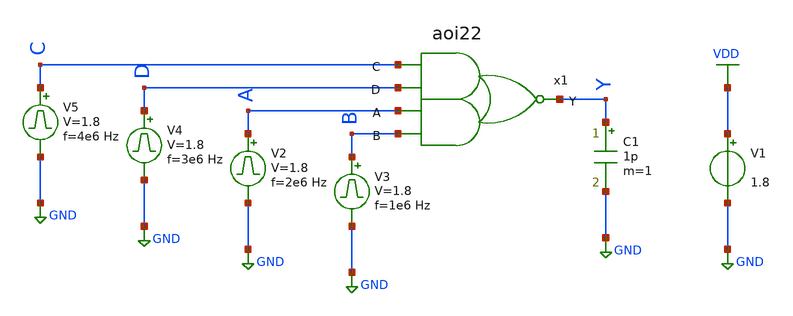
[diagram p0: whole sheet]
** sch_path: library/xschem/aoi22_tb.sch
**.subckt aoi22_tb
V1 VDD GND 1.8
V2 A GND pulse 0 1.8 '0.495/ 2e6 ' '0.01/2e6 ' '0.01/2e6 ' '0.49/2e6 ' '1/2e6 '
C1 Y GND 1p m=1
V3 B GND pulse 0 1.8 '0.495/ 1e6 ' '0.01/1e6 ' '0.01/1e6 ' '0.49/1e6 ' '1/1e6 '
V4 D GND pulse 0 1.8 '0.495/ 3e6 ' '0.01/3e6 ' '0.01/3e6 ' '0.49/3e6 ' '1/3e6 '
V5 C GND pulse 0 1.8 '0.495/ 4e6 ' '0.01/4e6 ' '0.01/4e6 ' '0.49/4e6 ' '1/4e6 '
x1 C D A Y B aoi22
**** begin user architecture code


.control
save all
tran 1n 2u
plot V(A) V(B)+2 V(C)+4 V(D)+6 V(Y)+8
.endc


** opencircuitdesign pdks install
.lib $::SKYWATER_MODELS/sky130.lib.spice tt


**** end user architecture code
**.ends

* expanding   symbol:  aoi22.sym # of pins=5
** sym_path: library/xschem/aoi22.sym
** sch_path: library/xschem/aoi22.sch
.subckt aoi22 C D A Y B
*.opin Y
*.ipin C
*.ipin D
*.ipin A
*.ipin B
XM1 Y A net2 GND sky130_fd_pr__nfet_01v8 L=0.15 W=1 nf=1 ad='int((nf+1)/2) * W/nf * 0.29' as='int((nf+2)/2) * W/nf * 0.29'
+ pd='2*int((nf+1)/2) * (W/nf + 0.29)' ps='2*int((nf+2)/2) * (W/nf + 0.29)' nrd='0.29 / W' nrs='0.29 / W'
+ sa=0 sb=0 sd=0 mult=1 m=1
XM2 net1 A VDD VDD sky130_fd_pr__pfet_01v8 L=0.15 W=1 nf=1 ad='int((nf+1)/2) * W/nf * 0.29' as='int((nf+2)/2) * W/nf * 0.29'
+ pd='2*int((nf+1)/2) * (W/nf + 0.29)' ps='2*int((nf+2)/2) * (W/nf + 0.29)' nrd='0.29 / W' nrs='0.29 / W'
+ sa=0 sb=0 sd=0 mult=1 m=1
XM4 net2 B GND GND sky130_fd_pr__nfet_01v8 L=0.15 W=1 nf=1 ad='int((nf+1)/2) * W/nf * 0.29' as='int((nf+2)/2) * W/nf * 0.29'
+ pd='2*int((nf+1)/2) * (W/nf + 0.29)' ps='2*int((nf+2)/2) * (W/nf + 0.29)' nrd='0.29 / W' nrs='0.29 / W'
+ sa=0 sb=0 sd=0 mult=1 m=1
XM3 net1 B VDD VDD sky130_fd_pr__pfet_01v8 L=0.15 W=1 nf=1 ad='int((nf+1)/2) * W/nf * 0.29' as='int((nf+2)/2) * W/nf * 0.29'
+ pd='2*int((nf+1)/2) * (W/nf + 0.29)' ps='2*int((nf+2)/2) * (W/nf + 0.29)' nrd='0.29 / W' nrs='0.29 / W'
+ sa=0 sb=0 sd=0 mult=1 m=1
XM5 Y C net1 VDD sky130_fd_pr__pfet_01v8 L=0.15 W=1 nf=1 ad='int((nf+1)/2) * W/nf * 0.29' as='int((nf+2)/2) * W/nf * 0.29'
+ pd='2*int((nf+1)/2) * (W/nf + 0.29)' ps='2*int((nf+2)/2) * (W/nf + 0.29)' nrd='0.29 / W' nrs='0.29 / W'
+ sa=0 sb=0 sd=0 mult=1 m=1
XM6 Y D net1 VDD sky130_fd_pr__pfet_01v8 L=0.15 W=1 nf=1 ad='int((nf+1)/2) * W/nf * 0.29' as='int((nf+2)/2) * W/nf * 0.29'
+ pd='2*int((nf+1)/2) * (W/nf + 0.29)' ps='2*int((nf+2)/2) * (W/nf + 0.29)' nrd='0.29 / W' nrs='0.29 / W'
+ sa=0 sb=0 sd=0 mult=1 m=1
XM7 Y C net3 GND sky130_fd_pr__nfet_01v8 L=0.15 W=1 nf=1 ad='int((nf+1)/2) * W/nf * 0.29' as='int((nf+2)/2) * W/nf * 0.29'
+ pd='2*int((nf+1)/2) * (W/nf + 0.29)' ps='2*int((nf+2)/2) * (W/nf + 0.29)' nrd='0.29 / W' nrs='0.29 / W'
+ sa=0 sb=0 sd=0 mult=1 m=1
XM8 net3 D GND GND sky130_fd_pr__nfet_01v8 L=0.15 W=1 nf=1 ad='int((nf+1)/2) * W/nf * 0.29' as='int((nf+2)/2) * W/nf * 0.29'
+ pd='2*int((nf+1)/2) * (W/nf + 0.29)' ps='2*int((nf+2)/2) * (W/nf + 0.29)' nrd='0.29 / W' nrs='0.29 / W'
+ sa=0 sb=0 sd=0 mult=1 m=1
.ends

.GLOBAL VDD
.GLOBAL GND
.end
